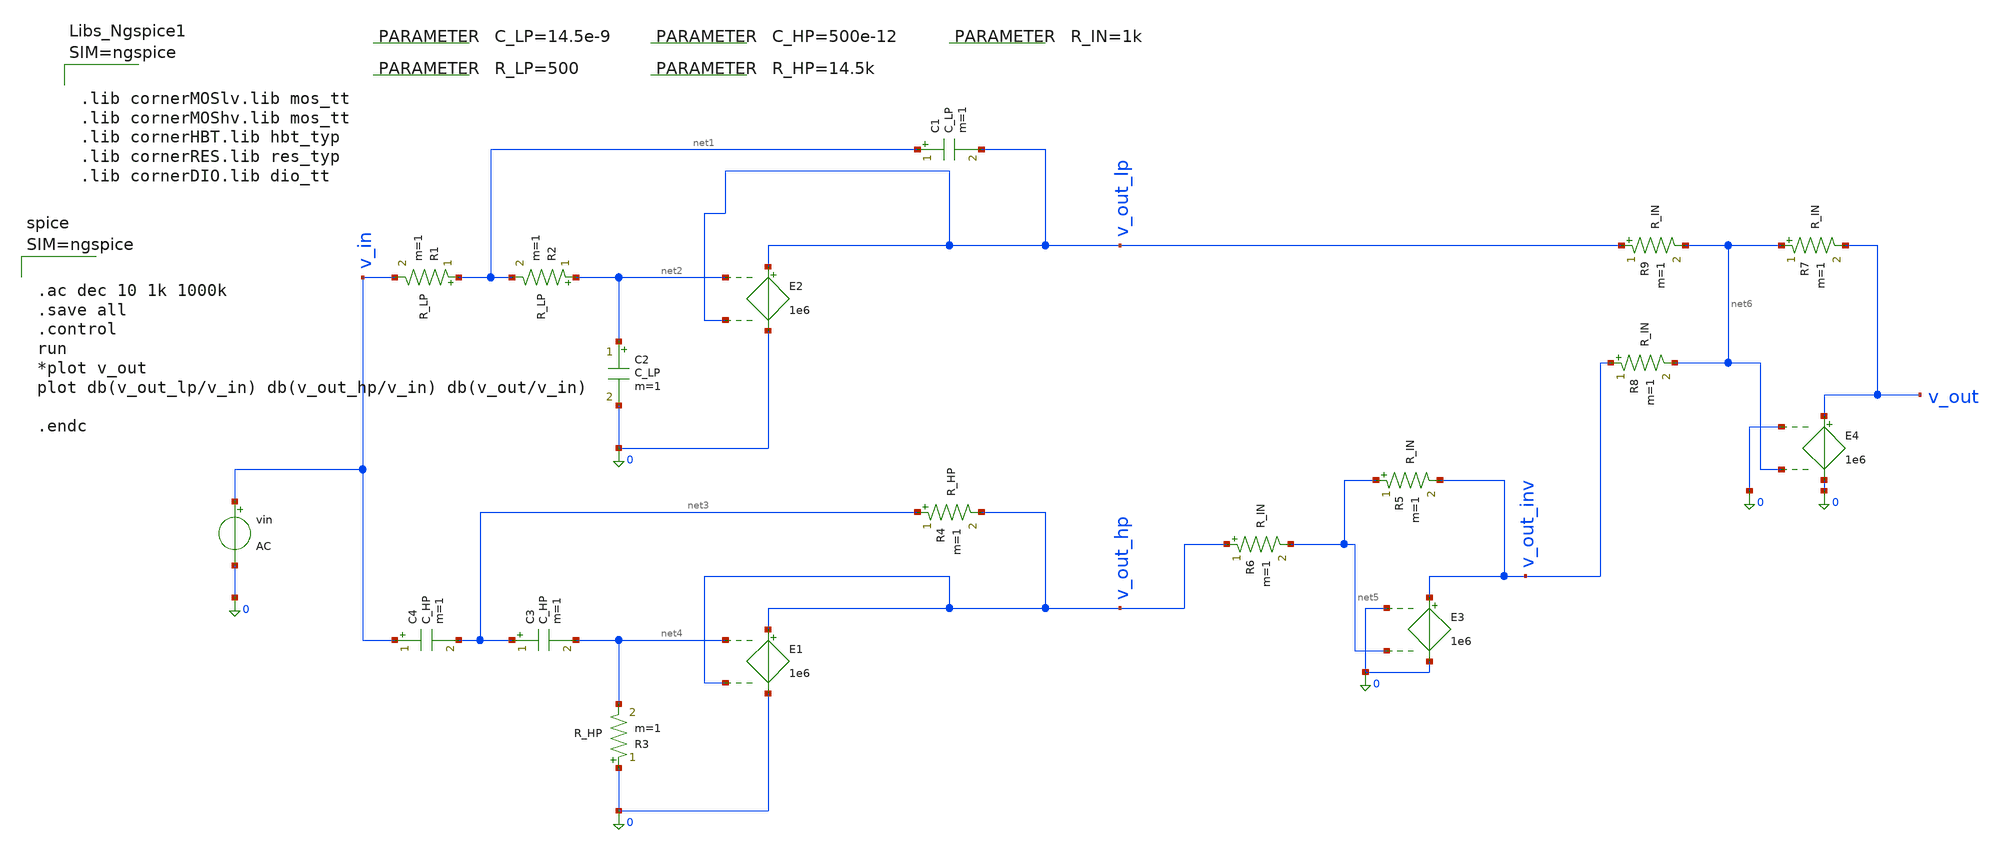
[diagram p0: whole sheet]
** sch_path: 001_Design/Ideal_Circuits/linkwitz_riley_cross_vsvc.sch
**.subckt linkwitz_riley_cross_vsvc
R1 net1 v_in R_LP m=1
R2 net2 net1 R_LP m=1
C1 net1 v_out_lp C_LP m=1
C2 net2 0 C_LP m=1
vin v_in 0 AC
.param C_LP=14.5e-9
.param R_LP=500
R3 0 net4 R_HP m=1
R4 net3 v_out_hp R_HP m=1
C3 net3 net4 C_HP m=1
C4 v_in net3 C_HP m=1
.param C_HP=500e-12
.param R_HP=14.5k
R5 net5 v_out_inv R_IN m=1
R6 v_out_hp net5 R_IN m=1
.param R_IN=1k
R7 net6 v_out R_IN m=1
R8 v_out_inv net6 R_IN m=1
R9 v_out_lp net6 R_IN m=1
E2 v_out_lp 0 net2 v_out_lp 1e6
E1 v_out_hp 0 net4 v_out_hp 1e6
E3 v_out_inv 0 0 net5 1e6
E4 v_out 0 0 net6 1e6
**** begin user architecture code



.lib cornerMOSlv.lib mos_tt
.lib cornerMOShv.lib mos_tt
.lib cornerHBT.lib hbt_typ
.lib cornerRES.lib res_typ
.lib cornerDIO.lib dio_tt






.ac dec 10 1k 1000k
.save all
.control
run
*plot v_out
plot db(v_out_lp/v_in) db(v_out_hp/v_in) db(v_out/v_in)

.endc



**** end user architecture code
**.ends
.end
